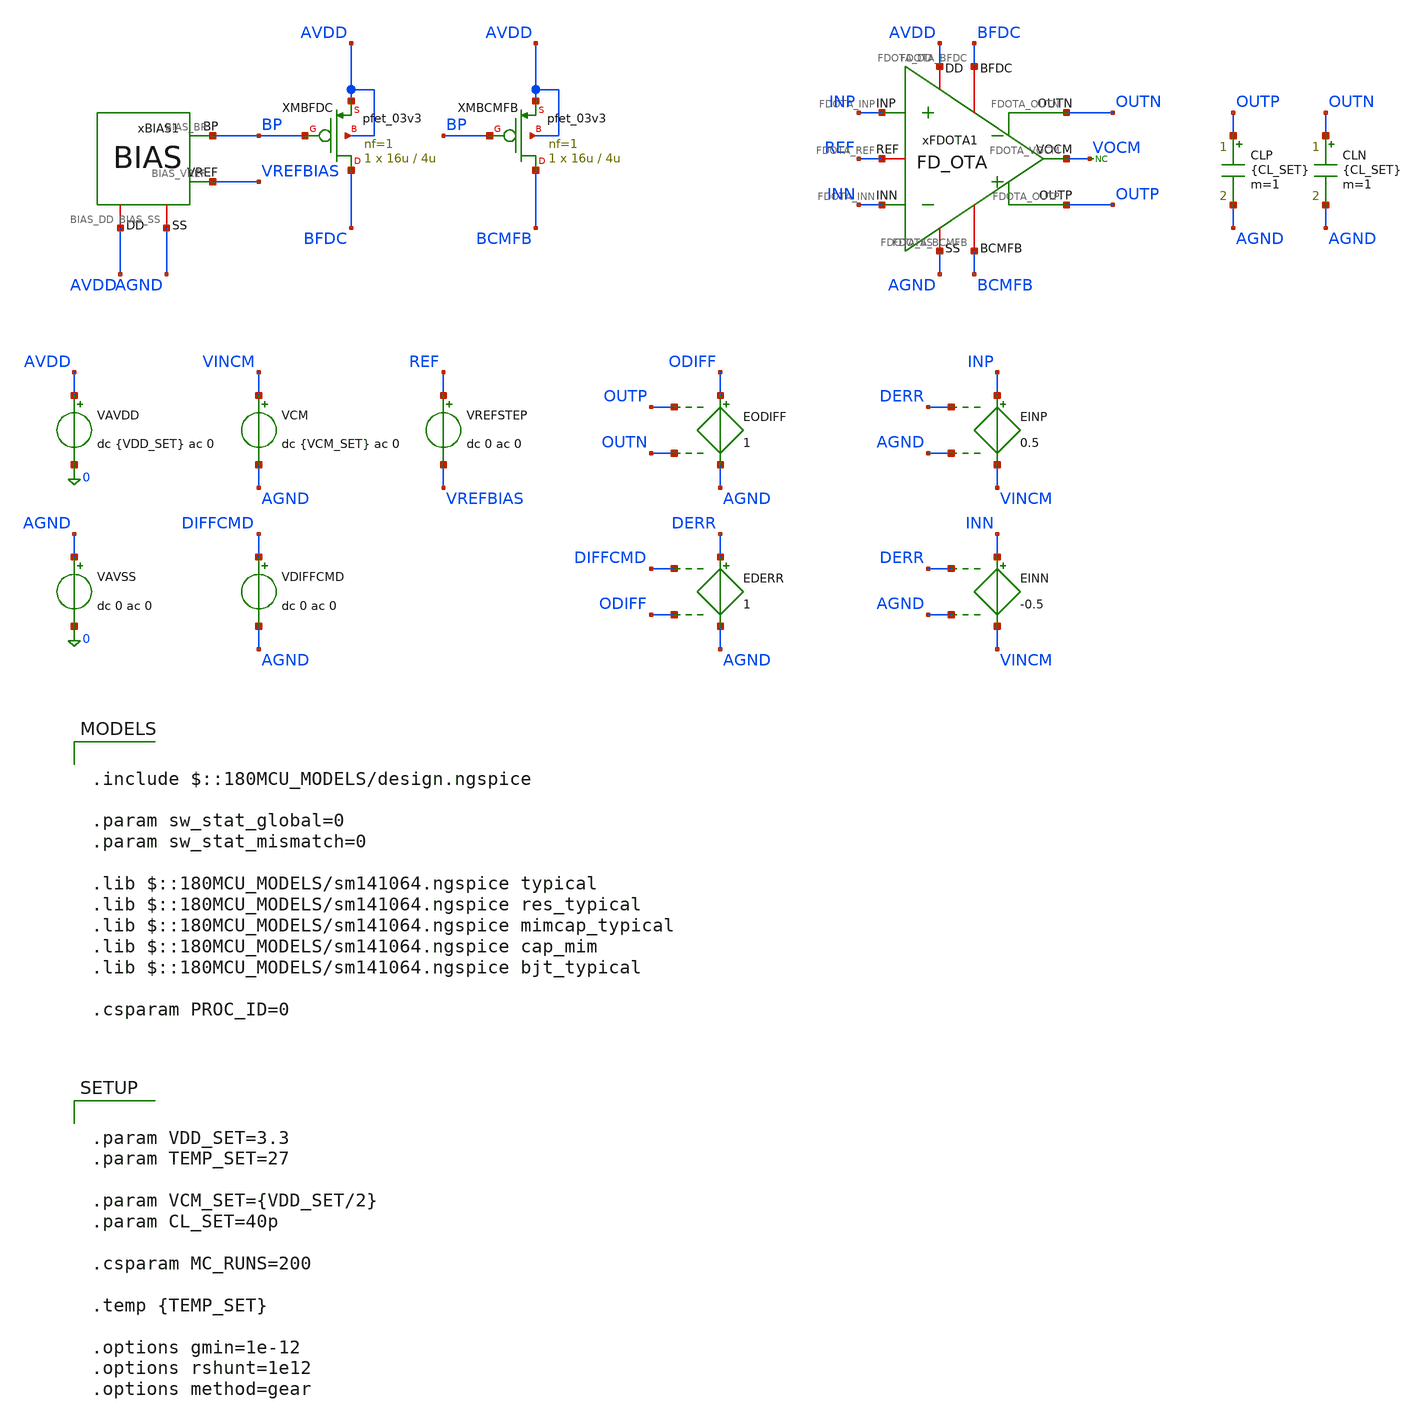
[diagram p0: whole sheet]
** sch_path: Design_Files/IC Design/Testbench/FD_OTA/Close_Loop/FD_OTA_TB_CL_NOM.sch
**.subckt FD_OTA_TB_CL_NOM
VAVDD AVDD 0 dc {VDD_SET} ac 0
.save i(vavdd)
VCM VINCM AGND dc {VCM_SET} ac 0
VREFSTEP REF VREFBIAS dc 0 ac 0
VAVSS AGND 0 dc 0 ac 0
VDIFFCMD DIFFCMD AGND dc 0 ac 0
CLP OUTP AGND {CL_SET} m=1
CLN OUTN AGND {CL_SET} m=1
* noconn VOCM
EODIFF ODIFF AGND OUTP OUTN 1
EDERR DERR AGND DIFFCMD ODIFF 1
xFDOTA1 AVDD AGND INP INN OUTN BFDC OUTP BCMFB REF VOCM FD_OTA
xBIAS1 AVDD AGND BP VREFBIAS BIAS
XMBFDC BFDC BP AVDD AVDD pfet_03v3 L=4u W=16u nf=1 ad='int((nf+1)/2) * W/nf * 0.18u' as='int((nf+2)/2) * W/nf * 0.18u'
+ pd='2*int((nf+1)/2) * (W/nf + 0.18u)' ps='2*int((nf+2)/2) * (W/nf + 0.18u)' nrd='0.18u / W' nrs='0.18u / W'
+ sa=0 sb=0 sd=0 m=1
XMBCMFB BCMFB BP AVDD AVDD pfet_03v3 L=4u W=16u nf=1 ad='int((nf+1)/2) * W/nf * 0.18u' as='int((nf+2)/2) * W/nf * 0.18u'
+ pd='2*int((nf+1)/2) * (W/nf + 0.18u)' ps='2*int((nf+2)/2) * (W/nf + 0.18u)' nrd='0.18u / W' nrs='0.18u / W'
+ sa=0 sb=0 sd=0 m=1
EINP INP VINCM DERR AGND 0.5
EINN INN VINCM DERR AGND -0.5
**** begin user architecture code

.include $::180MCU_MODELS/design.ngspice

.param sw_stat_global=0
.param sw_stat_mismatch=0

.lib $::180MCU_MODELS/sm141064.ngspice typical
.lib $::180MCU_MODELS/sm141064.ngspice res_typical
.lib $::180MCU_MODELS/sm141064.ngspice mimcap_typical
.lib $::180MCU_MODELS/sm141064.ngspice cap_mim
.lib $::180MCU_MODELS/sm141064.ngspice bjt_typical

.csparam PROC_ID=0




.control

destroy all

set noaskquit
set wr_singlescale
unset wr_vecnames

option klu
option numdgt=15
option method=gear
option maxord=2
option plotwinsize=0


if $&PROC_ID = 0
set proc=NOM
else
if $&PROC_ID = 1
set proc=FF
else
if $&PROC_ID = 2
set proc=SS
else
if $&PROC_ID = 3
set proc=FS
else
set proc=SF
end
end
end
end


shell mkdir -p /foss/designs/ECG_Acquisition_IC/Measurement_Results/IC_Simulation/FD_OTA/{$proc}.Result_txt
shell rm -f /foss/designs/ECG_Acquisition_IC/Measurement_Results/IC_Simulation/FD_OTA/{$proc}.Result_txt/{$proc}.cl_*.txt


foreach vddval 3.3 3.0 3.6

foreach tval 27 -40 125


if $vddval = 3.3

if $tval = 27
set case=nom
else
if $tval = -40
set case=tl
else
set case=th
end
end

else

if $vddval = 3.0

if $tval = 27
set case=vl
else
if $tval = -40
set case=vltl
else
set case=vlth
end
end

else

if $tval = 27
set case=vh
else
if $tval = -40
set case=vhtl
else
set case=vhth
end
end

end

end


alterparam VDD_SET=$vddval
alterparam TEMP_SET=$tval

reset

option klu
option numdgt=15
option method=gear
option maxord=2
option plotwinsize=0
option rshunt=1e12


* OP

save AVDD AGND INP INN OUTP OUTN REF VOCM DIFFCMD VREFBIAS
save vavdd#branch
save @m.xmbfdc.m0[id]
save @m.xmbcmfb.m0[id]

op

let vdd=v(AVDD)-v(AGND)

let vinp=v(INP)-v(AGND)
let vinn=v(INN)-v(AGND)
let vin_diff=vinp-vinn

let voutp=v(OUTP)-v(AGND)
let voutn=v(OUTN)-v(AGND)

let voutcm=0.5*(voutp+voutn)
let voutdiff=voutp-voutn

let vref=v(REF)-v(AGND)
let vocm=v(VOCM)-v(AGND)

let idd_total=abs(vavdd#branch)

let ibias_fdc=abs(@m.xmbfdc.m0[id])
let ibias_cmfb=abs(@m.xmbcmfb.m0[id])

wrdata /foss/designs/ECG_Acquisition_IC/Measurement_Results/IC_Simulation/FD_OTA/{$proc}.Result_txt/{$proc}.cl_{$case}_op.txt
+ vdd vinp vinn vin_diff voutp voutn voutcm voutdiff vref vocm idd_total ibias_fdc ibias_cmfb

destroy all


* DIFF DC

let vdiff_low=-$vddval
let vdiff_high=$vddval

save AGND INP INN OUTP OUTN REF VOCM DIFFCMD
save vavdd#branch
save @m.xmbfdc.m0[id]
save @m.xmbcmfb.m0[id]

dc VDIFFCMD $&vdiff_low $&vdiff_high 5m

let cl_cmd=v(DIFFCMD)-v(AGND)

let cl_vin_diff=v(INP)-v(INN)

let cl_voutp=v(OUTP)-v(AGND)
let cl_voutn=v(OUTN)-v(AGND)

let cl_voutcm=0.5*(cl_voutp+cl_voutn)
let cl_voutdiff=cl_voutp-cl_voutn

let cl_err=cl_voutdiff-cl_cmd

let cl_vocm=v(VOCM)-v(AGND)
let cl_vref=v(REF)-v(AGND)

let cl_idd=abs(vavdd#branch)

let cl_ibias_fdc=abs(@m.xmbfdc.m0[id])
let cl_ibias_cmfb=abs(@m.xmbcmfb.m0[id])

setscale cl_cmd

wrdata /foss/designs/ECG_Acquisition_IC/Measurement_Results/IC_Simulation/FD_OTA/{$proc}.Result_txt/{$proc}.cl_{$case}_diff_dc.txt
+ cl_vin_diff cl_voutp cl_voutn cl_voutcm cl_voutdiff cl_err cl_vocm cl_vref cl_idd cl_ibias_fdc cl_ibias_cmfb

destroy all


* ICMR -10m

option klu
option method=gear
option maxord=2
option itl1=1000
option itl2=5000
option rshunt=1e10

alter VDIFFCMD -10m

save AGND INP INN OUTP OUTN REF VOCM DIFFCMD
save vavdd#branch
save @m.xmbfdc.m0[id]
save @m.xmbcmfb.m0[id]

dc VCM $vddval 0 -5m

let icmr_cmd=v(DIFFCMD)-v(AGND)

let icmr_vin_cm=0.5*(v(INP)+v(INN))-v(AGND)
let icmr_vin_diff=v(INP)-v(INN)

let icmr_voutp=v(OUTP)-v(AGND)
let icmr_voutn=v(OUTN)-v(AGND)

let icmr_voutcm=0.5*(icmr_voutp+icmr_voutn)
let icmr_voutdiff=icmr_voutp-icmr_voutn

let icmr_vocm=v(VOCM)-v(AGND)
let icmr_vref=v(REF)-v(AGND)

let icmr_idd=abs(vavdd#branch)

let icmr_ibias_fdc=abs(@m.xmbfdc.m0[id])
let icmr_ibias_cmfb=abs(@m.xmbcmfb.m0[id])

setscale icmr_vin_cm

unset appendwrite

wrdata /foss/designs/ECG_Acquisition_IC/Measurement_Results/IC_Simulation/FD_OTA/{$proc}.Result_txt/{$proc}.cl_{$case}_icmr.txt
+ icmr_cmd icmr_vin_diff icmr_voutp icmr_voutn icmr_voutcm icmr_voutdiff icmr_vocm icmr_vref icmr_idd icmr_ibias_fdc
+ icmr_ibias_cmfb

destroy all


* ICMR +10m

alter VDIFFCMD 10m

save AGND INP INN OUTP OUTN REF VOCM DIFFCMD
save vavdd#branch
save @m.xmbfdc.m0[id]
save @m.xmbcmfb.m0[id]

dc VCM $vddval 0 -5m

let icmr_cmd=v(DIFFCMD)-v(AGND)

let icmr_vin_cm=0.5*(v(INP)+v(INN))-v(AGND)
let icmr_vin_diff=v(INP)-v(INN)

let icmr_voutp=v(OUTP)-v(AGND)
let icmr_voutn=v(OUTN)-v(AGND)

let icmr_voutcm=0.5*(icmr_voutp+icmr_voutn)
let icmr_voutdiff=icmr_voutp-icmr_voutn

let icmr_vocm=v(VOCM)-v(AGND)
let icmr_vref=v(REF)-v(AGND)

let icmr_idd=abs(vavdd#branch)

let icmr_ibias_fdc=abs(@m.xmbfdc.m0[id])
let icmr_ibias_cmfb=abs(@m.xmbcmfb.m0[id])

setscale icmr_vin_cm

set appendwrite

wrdata /foss/designs/ECG_Acquisition_IC/Measurement_Results/IC_Simulation/FD_OTA/{$proc}.Result_txt/{$proc}.cl_{$case}_icmr.txt
+ icmr_cmd icmr_vin_diff icmr_voutp icmr_voutn icmr_voutcm icmr_voutdiff icmr_vocm icmr_vref icmr_idd icmr_ibias_fdc
+ icmr_ibias_cmfb

unset appendwrite

destroy all


* DIFF TRAN

reset

option klu
option numdgt=15
option method=gear
option maxord=2
option plotwinsize=0
option rshunt=1e12

alter @VDIFFCMD[PWL]=[ 0 0 1u 0 1.001u 1.0 11u 1.0 11.001u 0 21u 0 21.001u -1.0 31u -1.0 31.001u 0
+ 40u 0 ]

save AGND INP INN OUTP OUTN REF VOCM DIFFCMD
save vavdd#branch
save @m.xmbfdc.m0[id]
save @m.xmbcmfb.m0[id]

tran 5n 40u

let tr_cmd=v(DIFFCMD)-v(AGND)

let tr_vin_diff=v(INP)-v(INN)

let tr_voutp=v(OUTP)-v(AGND)
let tr_voutn=v(OUTN)-v(AGND)

let tr_voutcm=0.5*(tr_voutp+tr_voutn)
let tr_voutdiff=tr_voutp-tr_voutn

let tr_err=tr_voutdiff-tr_cmd

let tr_vocm=v(VOCM)-v(AGND)
let tr_vref=v(REF)-v(AGND)

let tr_idd=abs(vavdd#branch)

let tr_ibias_fdc=abs(@m.xmbfdc.m0[id])
let tr_ibias_cmfb=abs(@m.xmbcmfb.m0[id])

setscale time

wrdata /foss/designs/ECG_Acquisition_IC/Measurement_Results/IC_Simulation/FD_OTA/{$proc}.Result_txt/{$proc}.cl_{$case}_diff_tran.txt
+ tr_cmd tr_vin_diff tr_voutp tr_voutn tr_voutcm tr_voutdiff tr_err tr_vocm tr_vref tr_idd tr_ibias_fdc
+ tr_ibias_cmfb

destroy all


* CM TRAN

reset

option klu
option numdgt=15
option method=gear
option maxord=2
option plotwinsize=0
option rshunt=1e12

alter @VREFSTEP[PWL]=[ 0 -0.8 1u -0.8 1.001u 0 11u 0 11.001u 0.8 21u 0.8 21.001u 0 40u 0 ]

save AGND OUTP OUTN REF VREFBIAS VOCM
save vavdd#branch
save @m.xmbfdc.m0[id]
save @m.xmbcmfb.m0[id]

tran 5n 40u

let cm_vref=v(REF)-v(AGND)
let cm_vrefbias=v(VREFBIAS)-v(AGND)

let cm_voutp=v(OUTP)-v(AGND)
let cm_voutn=v(OUTN)-v(AGND)

let cm_voutcm=0.5*(cm_voutp+cm_voutn)
let cm_voutdiff=cm_voutp-cm_voutn

let cm_vocm=v(VOCM)-v(AGND)

let cm_err=cm_voutcm-cm_vref

let cm_idd=abs(vavdd#branch)

let cm_ibias_fdc=abs(@m.xmbfdc.m0[id])
let cm_ibias_cmfb=abs(@m.xmbcmfb.m0[id])

setscale time

wrdata /foss/designs/ECG_Acquisition_IC/Measurement_Results/IC_Simulation/FD_OTA/{$proc}.Result_txt/{$proc}.cl_{$case}_cm_tran.txt
+ cm_vref cm_vrefbias cm_voutp cm_voutn cm_voutcm cm_voutdiff cm_vocm cm_err cm_idd cm_ibias_fdc cm_ibias_cmfb

destroy all


end
end


quit

.endc




.param VDD_SET=3.3
.param TEMP_SET=27

.param VCM_SET={VDD_SET/2}
.param CL_SET=40p

.csparam MC_RUNS=200

.temp {TEMP_SET}

.options gmin=1e-12
.options rshunt=1e12
.options method=gear


**** end user architecture code
**.ends
.end
